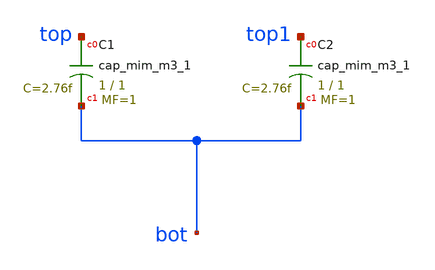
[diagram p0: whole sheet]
** sch_path: projects/mim_capacitor/xschem_ngspice/mimcap_xschem.sch
**.subckt mimcap_xschem
XC1 top bot sky130_fd_pr__cap_mim_m3_1 W=1 L=1 MF=1 m=1
XC2 top1 bot sky130_fd_pr__cap_mim_m3_1 W=1 L=1 MF=1 m=1
**.ends
.end
